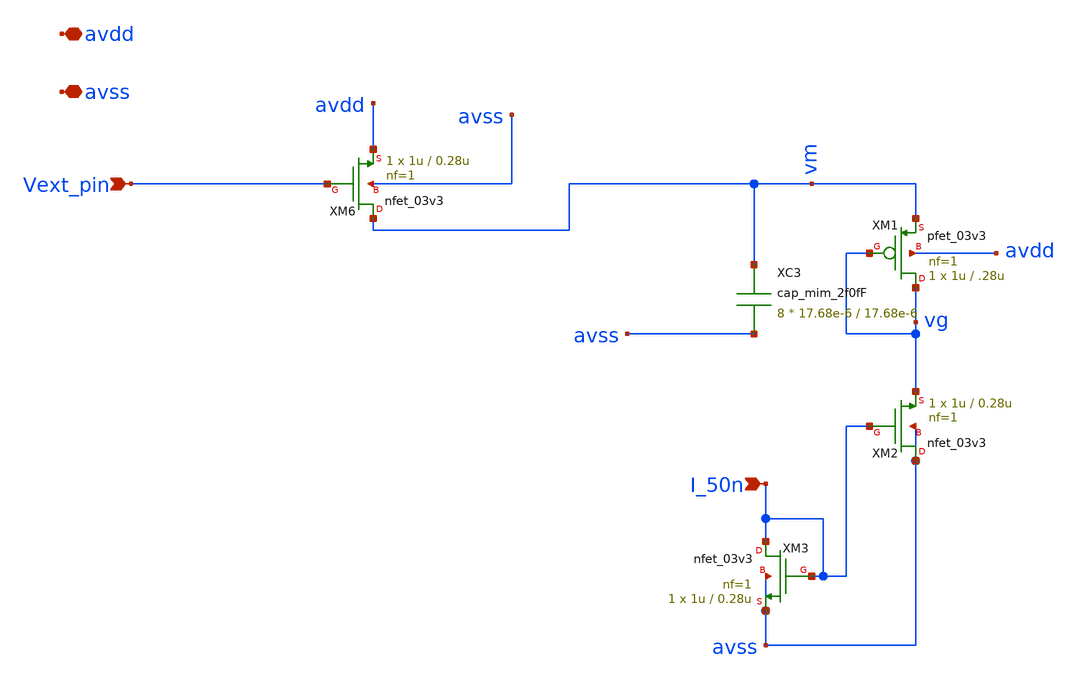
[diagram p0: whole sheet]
** sch_path: sch/integrator/integrator_final_mike.sch
**.subckt integrator_final_mike Vext_pin avdd avss I_50n
*.ipin Vext_pin
*.iopin avdd
*.iopin avss
*.ipin I_50n
XM1 vg vg vm avdd pfet_03v3 L=.28u W=1u nf=1 ad='int((nf+1)/2) * W/nf * 0.18u' as='int((nf+2)/2) * W/nf * 0.18u'
+ pd='2*int((nf+1)/2) * (W/nf + 0.18u)' ps='2*int((nf+2)/2) * (W/nf + 0.18u)' nrd='0.18u / W' nrs='0.18u / W'
+ sa=0 sb=0 sd=0 m=1
XM6 vm Vext_pin avdd avss nfet_03v3 L=0.28u W=1u nf=1 ad='int((nf+1)/2) * W/nf * 0.18u' as='int((nf+2)/2) * W/nf * 0.18u'
+ pd='2*int((nf+1)/2) * (W/nf + 0.18u)' ps='2*int((nf+2)/2) * (W/nf + 0.18u)' nrd='0.18u / W' nrs='0.18u / W'
+ sa=0 sb=0 sd=0 m=1
XM2 avss I_50n vg avss nfet_03v3 L=0.28u W=1u nf=1 ad='int((nf+1)/2) * W/nf * 0.18u' as='int((nf+2)/2) * W/nf * 0.18u'
+ pd='2*int((nf+1)/2) * (W/nf + 0.18u)' ps='2*int((nf+2)/2) * (W/nf + 0.18u)' nrd='0.18u / W' nrs='0.18u / W'
+ sa=0 sb=0 sd=0 m=1
XM3 I_50n I_50n avss avss nfet_03v3 L=0.28u W=1u nf=1 ad='int((nf+1)/2) * W/nf * 0.18u' as='int((nf+2)/2) * W/nf * 0.18u'
+ pd='2*int((nf+1)/2) * (W/nf + 0.18u)' ps='2*int((nf+2)/2) * (W/nf + 0.18u)' nrd='0.18u / W' nrs='0.18u / W'
+ sa=0 sb=0 sd=0 m=1
XC3 vm avss cap_mim_2f0fF c_width=17.68e-6 c_length=17.68e-6 m=8
**.ends
.end
